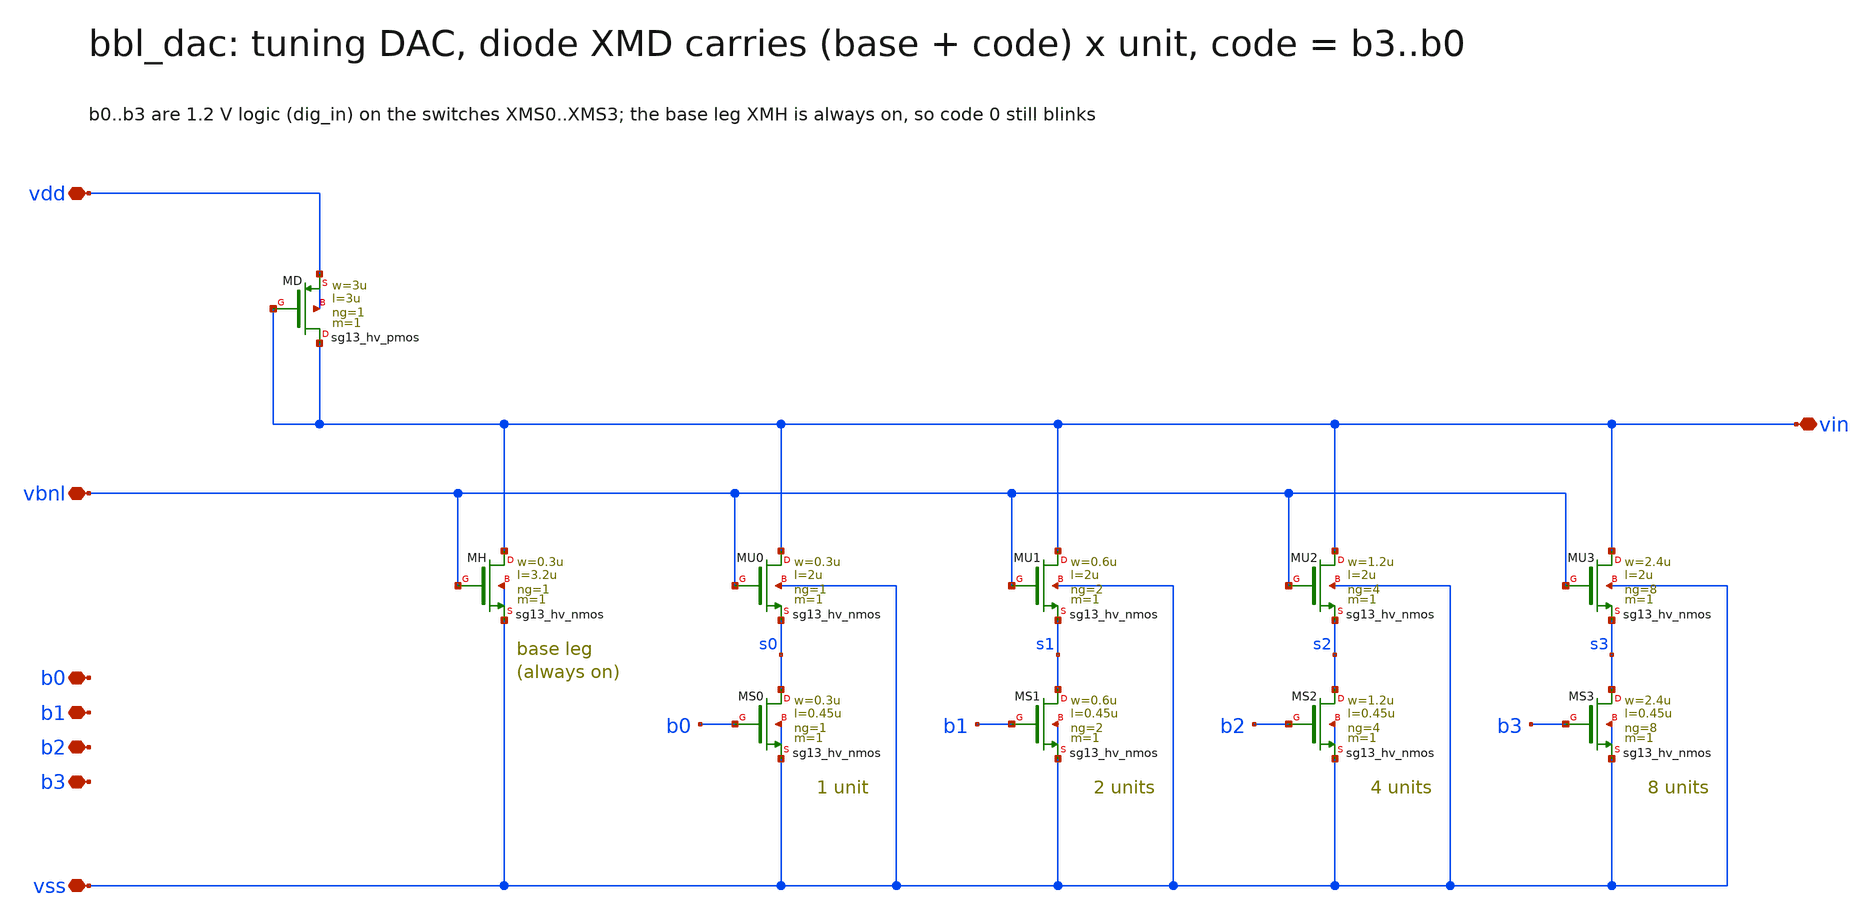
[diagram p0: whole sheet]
** sch_path: schematic/xschem/bbl_dac.sch
**.subckt bbl_dac vdd vss vin vbnl b0 b1 b2 b3
*.iopin vdd
*.iopin vss
*.iopin vin
*.iopin vbnl
*.iopin b0
*.iopin b1
*.iopin b2
*.iopin b3
XMD vin vin vdd vdd sg13_hv_pmos w=3u l=3u ng=1 m=1 mm_ok=1
XMH vin vbnl vss vss sg13_hv_nmos w=0.3u l=3.2u ng=1 m=1 mm_ok=1
XMU0 vin vbnl s0 vss sg13_hv_nmos w=0.3u l=2u ng=1 m=1 mm_ok=1
XMS0 s0 b0 vss vss sg13_hv_nmos w=0.3u l=0.45u ng=1 m=1 mm_ok=1
XMU1 vin vbnl s1 vss sg13_hv_nmos w=0.6u l=2u ng=2 m=1 mm_ok=1
XMS1 s1 b1 vss vss sg13_hv_nmos w=0.6u l=0.45u ng=2 m=1 mm_ok=1
XMU2 vin vbnl s2 vss sg13_hv_nmos w=1.2u l=2u ng=4 m=1 mm_ok=1
XMS2 s2 b2 vss vss sg13_hv_nmos w=1.2u l=0.45u ng=4 m=1 mm_ok=1
XMU3 vin vbnl s3 vss sg13_hv_nmos w=2.4u l=2u ng=8 m=1 mm_ok=1
XMS3 s3 b3 vss vss sg13_hv_nmos w=2.4u l=0.45u ng=8 m=1 mm_ok=1
**.ends
.end
